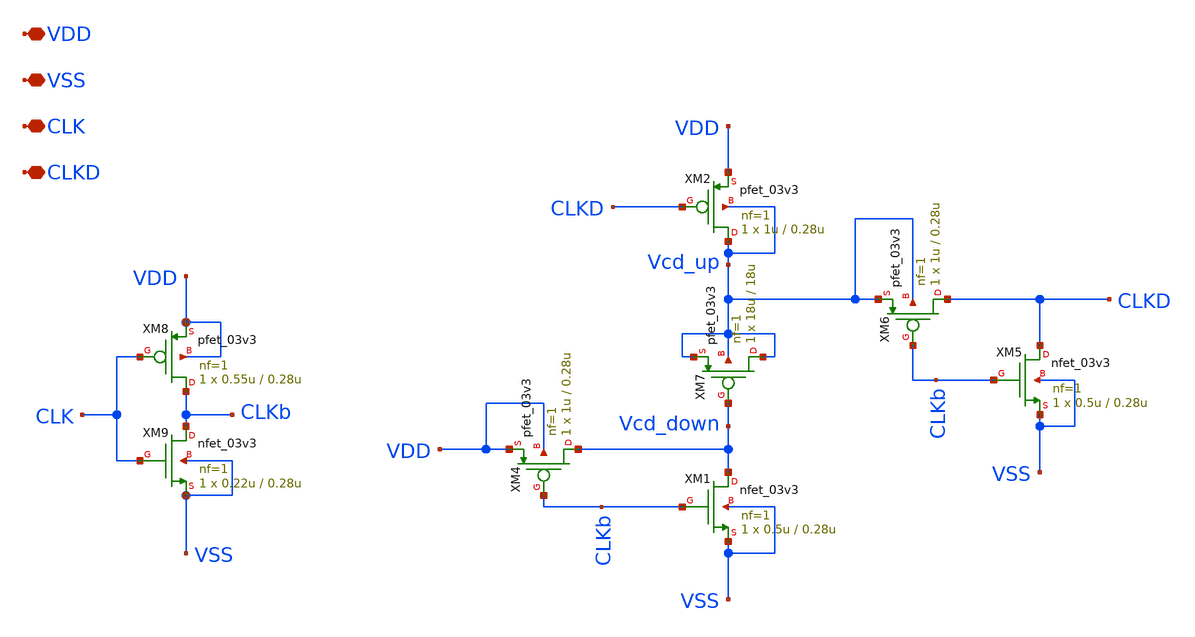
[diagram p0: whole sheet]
** sch_path: designs/DS_modulator/doubler/xschem/doubler.sch
**.subckt doubler VDD VSS CLK CLKD
*.iopin VDD
*.iopin VSS
*.iopin CLK
*.iopin CLKD
XM4 Vcd_down CLKb VDD VDD pfet_03v3 L=0.28u W=1u nf=1 ad='int((nf+1)/2) * W/nf * 0.18u' as='int((nf+2)/2) * W/nf * 0.18u'
+ pd='2*int((nf+1)/2) * (W/nf + 0.18u)' ps='2*int((nf+2)/2) * (W/nf + 0.18u)' nrd='0.18u / W' nrs='0.18u / W'
+ sa=0 sb=0 sd=0 m=1
XM5 CLKD CLKb VSS VSS nfet_03v3 L=0.28u W=0.5u nf=1 ad='int((nf+1)/2) * W/nf * 0.18u' as='int((nf+2)/2) * W/nf * 0.18u'
+ pd='2*int((nf+1)/2) * (W/nf + 0.18u)' ps='2*int((nf+2)/2) * (W/nf + 0.18u)' nrd='0.18u / W' nrs='0.18u / W'
+ sa=0 sb=0 sd=0 m=1
XM6 CLKD CLKb Vcd_up Vcd_up pfet_03v3 L=0.28u W=1u nf=1 ad='int((nf+1)/2) * W/nf * 0.18u' as='int((nf+2)/2) * W/nf * 0.18u'
+ pd='2*int((nf+1)/2) * (W/nf + 0.18u)' ps='2*int((nf+2)/2) * (W/nf + 0.18u)' nrd='0.18u / W' nrs='0.18u / W'
+ sa=0 sb=0 sd=0 m=1
XM2 Vcd_up CLKD VDD Vcd_up pfet_03v3 L=0.28u W=1u nf=1 ad='int((nf+1)/2) * W/nf * 0.18u' as='int((nf+2)/2) * W/nf * 0.18u'
+ pd='2*int((nf+1)/2) * (W/nf + 0.18u)' ps='2*int((nf+2)/2) * (W/nf + 0.18u)' nrd='0.18u / W' nrs='0.18u / W'
+ sa=0 sb=0 sd=0 m=1
XM8 CLKb CLK VDD VDD pfet_03v3 L=0.28u W=0.55u nf=1 ad='int((nf+1)/2) * W/nf * 0.18u' as='int((nf+2)/2) * W/nf * 0.18u'
+ pd='2*int((nf+1)/2) * (W/nf + 0.18u)' ps='2*int((nf+2)/2) * (W/nf + 0.18u)' nrd='0.18u / W' nrs='0.18u / W'
+ sa=0 sb=0 sd=0 m=1
XM9 CLKb CLK VSS VSS nfet_03v3 L=0.28u W=0.22u nf=1 ad='int((nf+1)/2) * W/nf * 0.18u' as='int((nf+2)/2) * W/nf * 0.18u'
+ pd='2*int((nf+1)/2) * (W/nf + 0.18u)' ps='2*int((nf+2)/2) * (W/nf + 0.18u)' nrd='0.18u / W' nrs='0.18u / W'
+ sa=0 sb=0 sd=0 m=1
XM7 Vcd_up Vcd_down Vcd_up Vcd_up pfet_03v3 L=18u W=18u nf=1 ad='int((nf+1)/2) * W/nf * 0.18u' as='int((nf+2)/2) * W/nf * 0.18u'
+ pd='2*int((nf+1)/2) * (W/nf + 0.18u)' ps='2*int((nf+2)/2) * (W/nf + 0.18u)' nrd='0.18u / W' nrs='0.18u / W'
+ sa=0 sb=0 sd=0 m=1
XM1 Vcd_down CLKb VSS VSS nfet_03v3 L=0.28u W=0.5u nf=1 ad='int((nf+1)/2) * W/nf * 0.18u' as='int((nf+2)/2) * W/nf * 0.18u'
+ pd='2*int((nf+1)/2) * (W/nf + 0.18u)' ps='2*int((nf+2)/2) * (W/nf + 0.18u)' nrd='0.18u / W' nrs='0.18u / W'
+ sa=0 sb=0 sd=0 m=1
**.ends
.end
